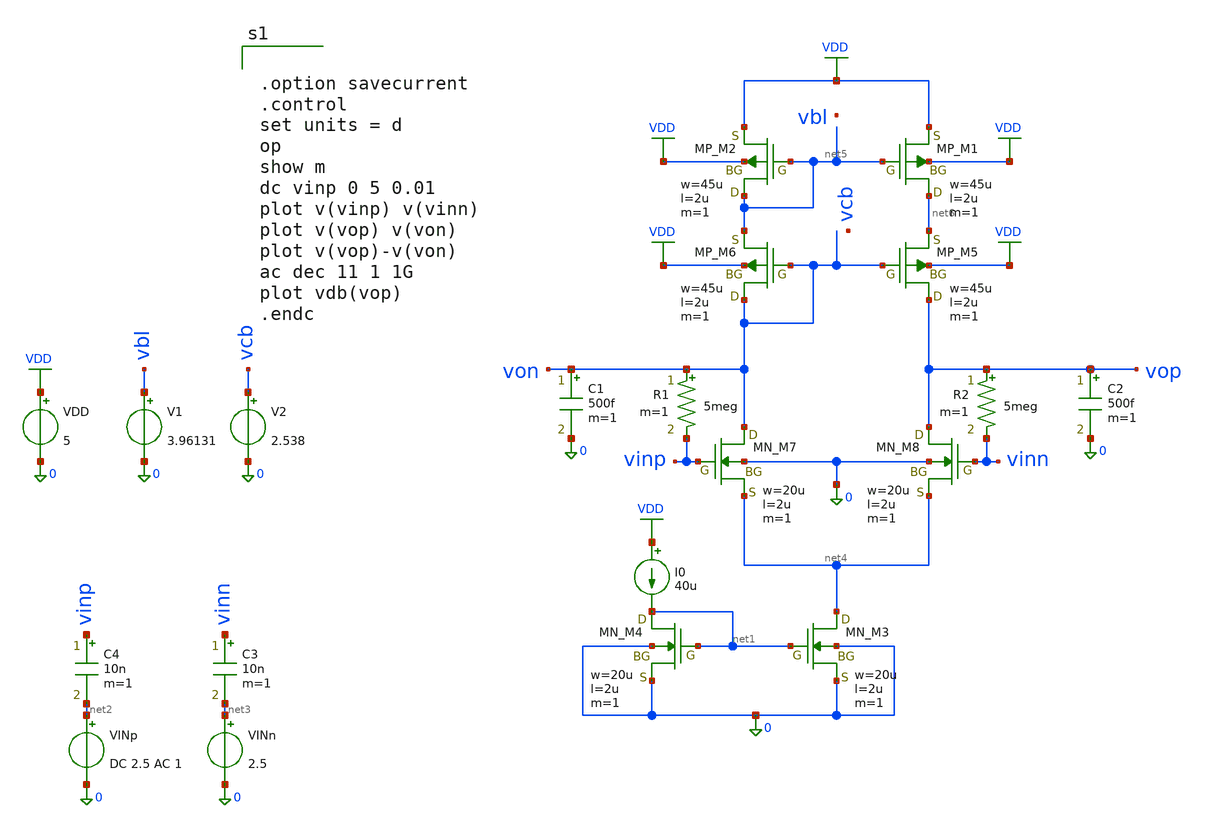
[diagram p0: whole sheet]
** sch_path: member_project/JJY_Receiver/Masahiro/jjy_recv/diff_amp/diff_cascode_nin_feedback.sch
**.subckt diff_cascode_nin_feedback
VDD VDD 0 5
VINp net2 0 DC 2.5 AC 1
I0 VDD net1 40u
C1 von 0 500f m=1
V1 vbl 0 3.96131
XM1 net6 net5 VDD VDD PMOS w=45u l=2u as=0 ad=0 ps=0 pd=0 nrd=0 nrs=0 m=1
XM2 net5 net5 VDD VDD PMOS w=45u l=2u as=0 ad=0 ps=0 pd=0 nrd=0 nrs=0 m=1
XM3 net4 net1 0 0 NMOS w=20u l=2u as=0 ad=0 ps=0 pd=0 nrd=0 nrs=0 m=1
XM4 net1 net1 0 0 NMOS w=20u l=2u as=0 ad=0 ps=0 pd=0 nrd=0 nrs=0 m=1
C2 vop 0 500f m=1
VINn net3 0 2.5
XM7 von vinp net4 0 NMOS w=20u l=2u as=0 ad=0 ps=0 pd=0 nrd=0 nrs=0 m=1
XM8 vop vinn net4 0 NMOS w=20u l=2u as=0 ad=0 ps=0 pd=0 nrd=0 nrs=0 m=1
XM5 vop von net6 VDD PMOS w=45u l=2u as=0 ad=0 ps=0 pd=0 nrd=0 nrs=0 m=1
XM6 von von net5 VDD PMOS w=45u l=2u as=0 ad=0 ps=0 pd=0 nrd=0 nrs=0 m=1
V2 vcb 0 2.538
R1 von vinp 5meg m=1
R2 vop vinn 5meg m=1
C3 vinn net3 10n m=1
C4 vinp net2 10n m=1
**** begin user architecture code
 .include $::LIB/ip62_models


.option savecurrent
.control
set units = d
op
show m
dc vinp 0 5 0.01
plot v(vinp) v(vinn)
plot v(vop) v(von)
plot v(vop)-v(von)
ac dec 11 1 1G
plot vdb(vop)
.endc


**** end user architecture code
**.ends
.GLOBAL VDD
.end
